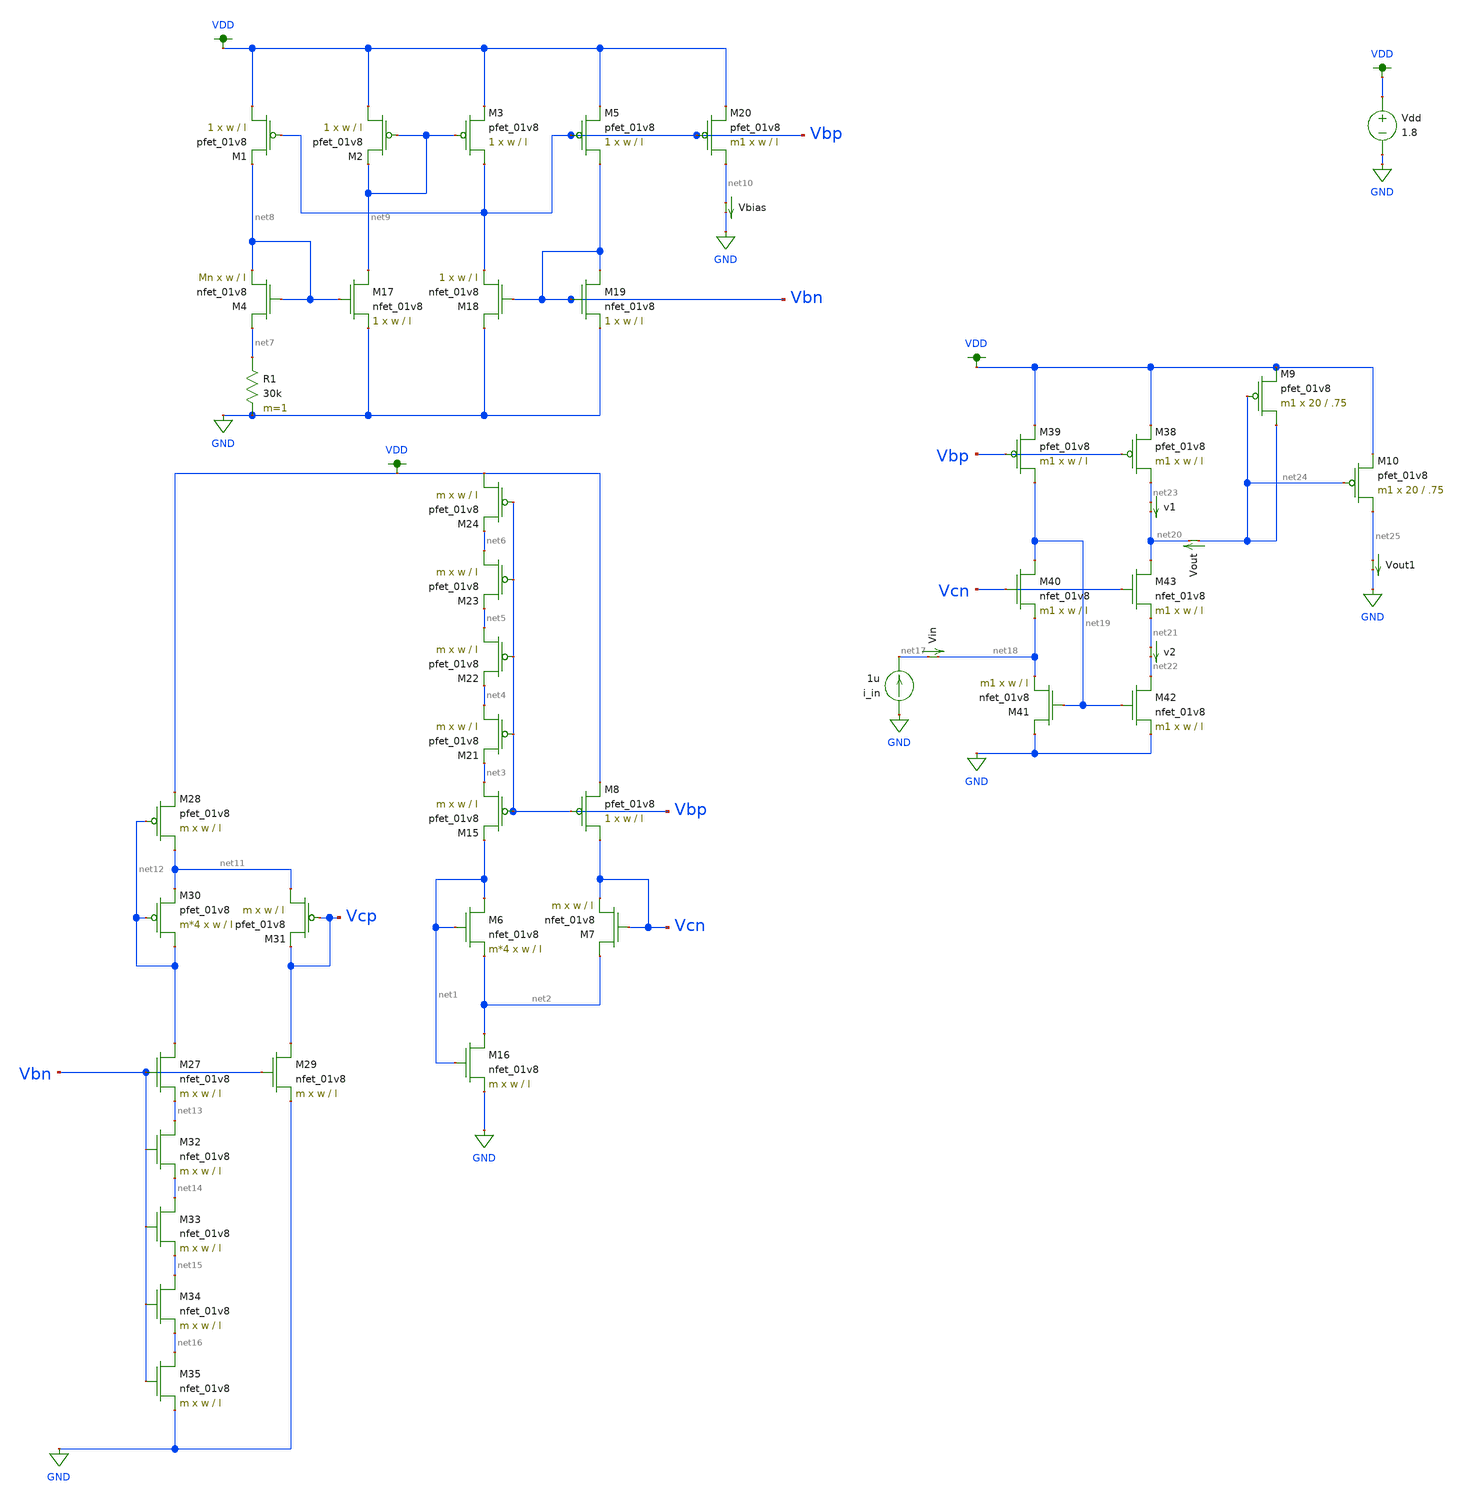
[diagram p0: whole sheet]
** sch_path: schematic/test/iout_mirror.sch
**.subckt iout_mirror
Vdd VDD GND 1.8
XM6 net1 net1 net2 GND sky130_fd_pr__nfet_01v8 L=l W=w nf=1 ad='int((nf+1)/2) * W/nf * 0.29' as='int((nf+2)/2) * W/nf * 0.29'
+ pd='2*int((nf+1)/2) * (W/nf + 0.29)' ps='2*int((nf+2)/2) * (W/nf + 0.29)' nrd='0.29 / W' nrs='0.29 / W'
+ sa=0 sb=0 sd=0 mult=m*4 m=m*4
XM7 net2 Vcn Vcn GND sky130_fd_pr__nfet_01v8 L=l W=w nf=1 ad='int((nf+1)/2) * W/nf * 0.29' as='int((nf+2)/2) * W/nf * 0.29'
+ pd='2*int((nf+1)/2) * (W/nf + 0.29)' ps='2*int((nf+2)/2) * (W/nf + 0.29)' nrd='0.29 / W' nrs='0.29 / W'
+ sa=0 sb=0 sd=0 mult=m m=m
XM8 Vcn Vbp VDD VDD sky130_fd_pr__pfet_01v8 L=l W=w nf=1 ad='int((nf+1)/2) * W/nf * 0.29' as='int((nf+2)/2) * W/nf * 0.29'
+ pd='2*int((nf+1)/2) * (W/nf + 0.29)' ps='2*int((nf+2)/2) * (W/nf + 0.29)' nrd='0.29 / W' nrs='0.29 / W'
+ sa=0 sb=0 sd=0 mult=1 m=1
XM15 net3 Vbp net1 VDD sky130_fd_pr__pfet_01v8 L=l W=w nf=1 ad='int((nf+1)/2) * W/nf * 0.29' as='int((nf+2)/2) * W/nf * 0.29'
+ pd='2*int((nf+1)/2) * (W/nf + 0.29)' ps='2*int((nf+2)/2) * (W/nf + 0.29)' nrd='0.29 / W' nrs='0.29 / W'
+ sa=0 sb=0 sd=0 mult=m m=m
XM16 net2 net1 GND GND sky130_fd_pr__nfet_01v8 L=l W=w nf=1 ad='int((nf+1)/2) * W/nf * 0.29' as='int((nf+2)/2) * W/nf * 0.29'
+ pd='2*int((nf+1)/2) * (W/nf + 0.29)' ps='2*int((nf+2)/2) * (W/nf + 0.29)' nrd='0.29 / W' nrs='0.29 / W'
+ sa=0 sb=0 sd=0 mult=m m=m
XM21 net4 Vbp net3 VDD sky130_fd_pr__pfet_01v8 L=l W=w nf=1 ad='int((nf+1)/2) * W/nf * 0.29' as='int((nf+2)/2) * W/nf * 0.29'
+ pd='2*int((nf+1)/2) * (W/nf + 0.29)' ps='2*int((nf+2)/2) * (W/nf + 0.29)' nrd='0.29 / W' nrs='0.29 / W'
+ sa=0 sb=0 sd=0 mult=m m=m
XM22 net5 Vbp net4 VDD sky130_fd_pr__pfet_01v8 L=l W=w nf=1 ad='int((nf+1)/2) * W/nf * 0.29' as='int((nf+2)/2) * W/nf * 0.29'
+ pd='2*int((nf+1)/2) * (W/nf + 0.29)' ps='2*int((nf+2)/2) * (W/nf + 0.29)' nrd='0.29 / W' nrs='0.29 / W'
+ sa=0 sb=0 sd=0 mult=m m=m
XM23 net6 Vbp net5 VDD sky130_fd_pr__pfet_01v8 L=l W=w nf=1 ad='int((nf+1)/2) * W/nf * 0.29' as='int((nf+2)/2) * W/nf * 0.29'
+ pd='2*int((nf+1)/2) * (W/nf + 0.29)' ps='2*int((nf+2)/2) * (W/nf + 0.29)' nrd='0.29 / W' nrs='0.29 / W'
+ sa=0 sb=0 sd=0 mult=m m=m
XM24 VDD Vbp net6 VDD sky130_fd_pr__pfet_01v8 L=l W=w nf=1 ad='int((nf+1)/2) * W/nf * 0.29' as='int((nf+2)/2) * W/nf * 0.29'
+ pd='2*int((nf+1)/2) * (W/nf + 0.29)' ps='2*int((nf+2)/2) * (W/nf + 0.29)' nrd='0.29 / W' nrs='0.29 / W'
+ sa=0 sb=0 sd=0 mult=m m=m
XM1 VDD Vbp net8 VDD sky130_fd_pr__pfet_01v8 L=l W=w nf=1 ad='int((nf+1)/2) * W/nf * 0.29' as='int((nf+2)/2) * W/nf * 0.29'
+ pd='2*int((nf+1)/2) * (W/nf + 0.29)' ps='2*int((nf+2)/2) * (W/nf + 0.29)' nrd='0.29 / W' nrs='0.29 / W'
+ sa=0 sb=0 sd=0 mult=1 m=1
XM2 VDD net9 net9 VDD sky130_fd_pr__pfet_01v8 L=l W=w nf=1 ad='int((nf+1)/2) * W/nf * 0.29' as='int((nf+2)/2) * W/nf * 0.29'
+ pd='2*int((nf+1)/2) * (W/nf + 0.29)' ps='2*int((nf+2)/2) * (W/nf + 0.29)' nrd='0.29 / W' nrs='0.29 / W'
+ sa=0 sb=0 sd=0 mult=1 m=1
XM3 Vbp net9 VDD VDD sky130_fd_pr__pfet_01v8 L=l W=w nf=1 ad='int((nf+1)/2) * W/nf * 0.29' as='int((nf+2)/2) * W/nf * 0.29'
+ pd='2*int((nf+1)/2) * (W/nf + 0.29)' ps='2*int((nf+2)/2) * (W/nf + 0.29)' nrd='0.29 / W' nrs='0.29 / W'
+ sa=0 sb=0 sd=0 mult=1 m=1
XM5 Vbn Vbp VDD VDD sky130_fd_pr__pfet_01v8 L=l W=w nf=1 ad='int((nf+1)/2) * W/nf * 0.29' as='int((nf+2)/2) * W/nf * 0.29'
+ pd='2*int((nf+1)/2) * (W/nf + 0.29)' ps='2*int((nf+2)/2) * (W/nf + 0.29)' nrd='0.29 / W' nrs='0.29 / W'
+ sa=0 sb=0 sd=0 mult=1 m=1
XM4 net7 net8 net8 GND sky130_fd_pr__nfet_01v8 L=l W=w nf=1 ad='int((nf+1)/2) * W/nf * 0.29' as='int((nf+2)/2) * W/nf * 0.29'
+ pd='2*int((nf+1)/2) * (W/nf + 0.29)' ps='2*int((nf+2)/2) * (W/nf + 0.29)' nrd='0.29 / W' nrs='0.29 / W'
+ sa=0 sb=0 sd=0 mult=Mn m=Mn
XM17 net9 net8 GND GND sky130_fd_pr__nfet_01v8 L=l W=w nf=1 ad='int((nf+1)/2) * W/nf * 0.29' as='int((nf+2)/2) * W/nf * 0.29'
+ pd='2*int((nf+1)/2) * (W/nf + 0.29)' ps='2*int((nf+2)/2) * (W/nf + 0.29)' nrd='0.29 / W' nrs='0.29 / W'
+ sa=0 sb=0 sd=0 mult=1 m=1
XM18 GND Vbn Vbp GND sky130_fd_pr__nfet_01v8 L=l W=w nf=1 ad='int((nf+1)/2) * W/nf * 0.29' as='int((nf+2)/2) * W/nf * 0.29'
+ pd='2*int((nf+1)/2) * (W/nf + 0.29)' ps='2*int((nf+2)/2) * (W/nf + 0.29)' nrd='0.29 / W' nrs='0.29 / W'
+ sa=0 sb=0 sd=0 mult=1 m=1
XM19 Vbn Vbn GND GND sky130_fd_pr__nfet_01v8 L=l W=w nf=1 ad='int((nf+1)/2) * W/nf * 0.29' as='int((nf+2)/2) * W/nf * 0.29'
+ pd='2*int((nf+1)/2) * (W/nf + 0.29)' ps='2*int((nf+2)/2) * (W/nf + 0.29)' nrd='0.29 / W' nrs='0.29 / W'
+ sa=0 sb=0 sd=0 mult=1 m=1
R1 net7 GND 30k m=1
XM20 net10 Vbp VDD VDD sky130_fd_pr__pfet_01v8 L=l W=w nf=1 ad='int((nf+1)/2) * W/nf * 0.29' as='int((nf+2)/2) * W/nf * 0.29'
+ pd='2*int((nf+1)/2) * (W/nf + 0.29)' ps='2*int((nf+2)/2) * (W/nf + 0.29)' nrd='0.29 / W' nrs='0.29 / W'
+ sa=0 sb=0 sd=0 mult=m1 m=m1
Vbias net10 GND 0
.save i(vbias)
XM27 net12 Vbn net13 GND sky130_fd_pr__nfet_01v8 L=l W=w nf=1 ad='int((nf+1)/2) * W/nf * 0.29' as='int((nf+2)/2) * W/nf * 0.29'
+ pd='2*int((nf+1)/2) * (W/nf + 0.29)' ps='2*int((nf+2)/2) * (W/nf + 0.29)' nrd='0.29 / W' nrs='0.29 / W'
+ sa=0 sb=0 sd=0 mult=m m=m
XM28 net11 net12 VDD VDD sky130_fd_pr__pfet_01v8 L=l W=w nf=1 ad='int((nf+1)/2) * W/nf * 0.29' as='int((nf+2)/2) * W/nf * 0.29'
+ pd='2*int((nf+1)/2) * (W/nf + 0.29)' ps='2*int((nf+2)/2) * (W/nf + 0.29)' nrd='0.29 / W' nrs='0.29 / W'
+ sa=0 sb=0 sd=0 mult=m m=m
XM29 Vcp Vbn GND GND sky130_fd_pr__nfet_01v8 L=l W=w nf=1 ad='int((nf+1)/2) * W/nf * 0.29' as='int((nf+2)/2) * W/nf * 0.29'
+ pd='2*int((nf+1)/2) * (W/nf + 0.29)' ps='2*int((nf+2)/2) * (W/nf + 0.29)' nrd='0.29 / W' nrs='0.29 / W'
+ sa=0 sb=0 sd=0 mult=m m=m
XM30 net12 net12 net11 VDD sky130_fd_pr__pfet_01v8 L=l W=w nf=1 ad='int((nf+1)/2) * W/nf * 0.29' as='int((nf+2)/2) * W/nf * 0.29'
+ pd='2*int((nf+1)/2) * (W/nf + 0.29)' ps='2*int((nf+2)/2) * (W/nf + 0.29)' nrd='0.29 / W' nrs='0.29 / W'
+ sa=0 sb=0 sd=0 mult=m*4 m=m*4
XM31 net11 Vcp Vcp VDD sky130_fd_pr__pfet_01v8 L=l W=w nf=1 ad='int((nf+1)/2) * W/nf * 0.29' as='int((nf+2)/2) * W/nf * 0.29'
+ pd='2*int((nf+1)/2) * (W/nf + 0.29)' ps='2*int((nf+2)/2) * (W/nf + 0.29)' nrd='0.29 / W' nrs='0.29 / W'
+ sa=0 sb=0 sd=0 mult=m m=m
XM32 net13 Vbn net14 GND sky130_fd_pr__nfet_01v8 L=l W=w nf=1 ad='int((nf+1)/2) * W/nf * 0.29' as='int((nf+2)/2) * W/nf * 0.29'
+ pd='2*int((nf+1)/2) * (W/nf + 0.29)' ps='2*int((nf+2)/2) * (W/nf + 0.29)' nrd='0.29 / W' nrs='0.29 / W'
+ sa=0 sb=0 sd=0 mult=m m=m
XM33 net14 Vbn net15 GND sky130_fd_pr__nfet_01v8 L=l W=w nf=1 ad='int((nf+1)/2) * W/nf * 0.29' as='int((nf+2)/2) * W/nf * 0.29'
+ pd='2*int((nf+1)/2) * (W/nf + 0.29)' ps='2*int((nf+2)/2) * (W/nf + 0.29)' nrd='0.29 / W' nrs='0.29 / W'
+ sa=0 sb=0 sd=0 mult=m m=m
XM34 net15 Vbn net16 GND sky130_fd_pr__nfet_01v8 L=l W=w nf=1 ad='int((nf+1)/2) * W/nf * 0.29' as='int((nf+2)/2) * W/nf * 0.29'
+ pd='2*int((nf+1)/2) * (W/nf + 0.29)' ps='2*int((nf+2)/2) * (W/nf + 0.29)' nrd='0.29 / W' nrs='0.29 / W'
+ sa=0 sb=0 sd=0 mult=m m=m
XM35 net16 Vbn GND GND sky130_fd_pr__nfet_01v8 L=l W=w nf=1 ad='int((nf+1)/2) * W/nf * 0.29' as='int((nf+2)/2) * W/nf * 0.29'
+ pd='2*int((nf+1)/2) * (W/nf + 0.29)' ps='2*int((nf+2)/2) * (W/nf + 0.29)' nrd='0.29 / W' nrs='0.29 / W'
+ sa=0 sb=0 sd=0 mult=m m=m
i_in GND net17 1u
Vout net24 net20 0
.save i(vout)
Vin net17 net18 0
.save i(vin)
XM38 net23 Vbp VDD VDD sky130_fd_pr__pfet_01v8 L=l W=w nf=1 ad='int((nf+1)/2) * W/nf * 0.29' as='int((nf+2)/2) * W/nf * 0.29'
+ pd='2*int((nf+1)/2) * (W/nf + 0.29)' ps='2*int((nf+2)/2) * (W/nf + 0.29)' nrd='0.29 / W' nrs='0.29 / W'
+ sa=0 sb=0 sd=0 mult=m1 m=m1
XM39 net19 Vbp VDD VDD sky130_fd_pr__pfet_01v8 L=l W=w nf=1 ad='int((nf+1)/2) * W/nf * 0.29' as='int((nf+2)/2) * W/nf * 0.29'
+ pd='2*int((nf+1)/2) * (W/nf + 0.29)' ps='2*int((nf+2)/2) * (W/nf + 0.29)' nrd='0.29 / W' nrs='0.29 / W'
+ sa=0 sb=0 sd=0 mult=m1 m=m1
XM40 net19 Vcn net18 GND sky130_fd_pr__nfet_01v8 L=l W=w nf=1 ad='int((nf+1)/2) * W/nf * 0.29' as='int((nf+2)/2) * W/nf * 0.29'
+ pd='2*int((nf+1)/2) * (W/nf + 0.29)' ps='2*int((nf+2)/2) * (W/nf + 0.29)' nrd='0.29 / W' nrs='0.29 / W'
+ sa=0 sb=0 sd=0 mult=m1 m=m1
v2 net21 net22 0
.save i(v2)
v1 net23 net20 0
.save i(v1)
Vout1 net25 GND 0
.save i(vout1)
XM41 GND net19 net18 GND sky130_fd_pr__nfet_01v8 L=l W=w nf=1 ad='int((nf+1)/2) * W/nf * 0.29' as='int((nf+2)/2) * W/nf * 0.29'
+ pd='2*int((nf+1)/2) * (W/nf + 0.29)' ps='2*int((nf+2)/2) * (W/nf + 0.29)' nrd='0.29 / W' nrs='0.29 / W'
+ sa=0 sb=0 sd=0 mult=m1 m=m1
XM42 net22 net19 GND GND sky130_fd_pr__nfet_01v8 L=l W=w nf=1 ad='int((nf+1)/2) * W/nf * 0.29' as='int((nf+2)/2) * W/nf * 0.29'
+ pd='2*int((nf+1)/2) * (W/nf + 0.29)' ps='2*int((nf+2)/2) * (W/nf + 0.29)' nrd='0.29 / W' nrs='0.29 / W'
+ sa=0 sb=0 sd=0 mult=m1 m=m1
XM43 net20 Vcn net21 GND sky130_fd_pr__nfet_01v8 L=l W=w nf=1 ad='int((nf+1)/2) * W/nf * 0.29' as='int((nf+2)/2) * W/nf * 0.29'
+ pd='2*int((nf+1)/2) * (W/nf + 0.29)' ps='2*int((nf+2)/2) * (W/nf + 0.29)' nrd='0.29 / W' nrs='0.29 / W'
+ sa=0 sb=0 sd=0 mult=m1 m=m1
XM9 net24 net24 VDD VDD sky130_fd_pr__pfet_01v8 L=.75 W=20 nf=1 ad='int((nf+1)/2) * W/nf * 0.29' as='int((nf+2)/2) * W/nf * 0.29'
+ pd='2*int((nf+1)/2) * (W/nf + 0.29)' ps='2*int((nf+2)/2) * (W/nf + 0.29)' nrd='0.29 / W' nrs='0.29 / W'
+ sa=0 sb=0 sd=0 mult=m1 m=m1
XM10 net25 net24 VDD VDD sky130_fd_pr__pfet_01v8 L=.75 W=20 nf=1 ad='int((nf+1)/2) * W/nf * 0.29' as='int((nf+2)/2) * W/nf * 0.29'
+ pd='2*int((nf+1)/2) * (W/nf + 0.29)' ps='2*int((nf+2)/2) * (W/nf + 0.29)' nrd='0.29 / W' nrs='0.29 / W'
+ sa=0 sb=0 sd=0 mult=m1 m=m1
**** begin user architecture code



.param m = 1
.param w = 10
.param l = 2
.param Mn = 8
.param m1 = 2

.control
set wr_vecnames
set wr_singlescale
save all
dc i_in 0 5u .001u
wrdata ~/Desktop/madvlsi/madvlsi_proj_4/data/iout_mirror6.txt i(Vin) i(Vout) i(Vbias) i(v1) i(v2)
+ i(Vout1) v(Vbp) v(Vcn)
.endc



.option wnflag=1
.param MC_SWITCH=0.0
.lib ~/skywater/skywater-pdk/libraries/sky130_fd_pr_ngspice/latest/models/sky130.lib.spice tt

**** end user architecture code
**.ends
.GLOBAL GND
.GLOBAL VDD
.end
